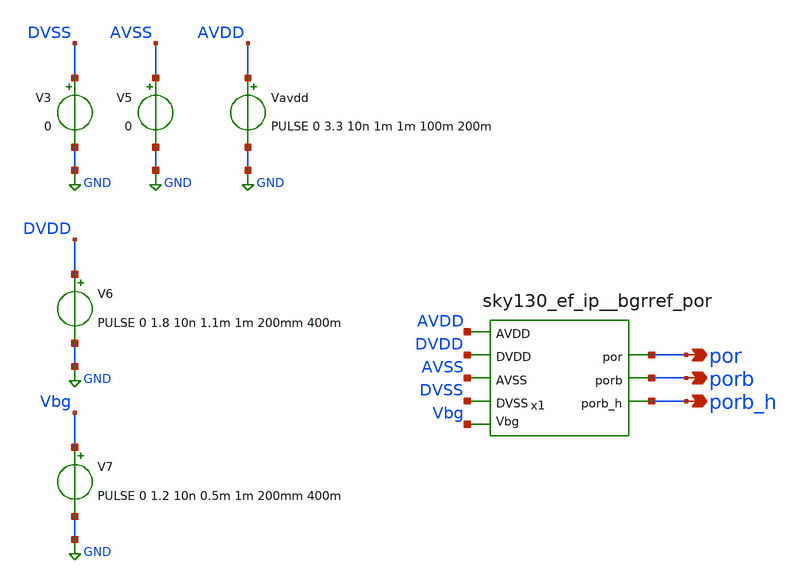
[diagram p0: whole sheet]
** sch_path: xschem/startup_sim.sch
**.subckt startup_sim por porb porb_h
*.opin por
*.opin porb
*.opin porb_h
x1 Vbg por AVSS AVDD DVDD porb DVSS porb_h VCC VSS sky130_ef_ip__bgrref_por W_N=1 L_N=0.2 W_P=1
+ L_P=0.2 m=1
V3 DVSS GND 0
Vavdd AVDD GND PULSE 0 3.3 10n 1m 1m 100m 200m
V5 AVSS GND 0
V6 DVDD GND PULSE 0 1.8 10n 1.1m 1m 200mm 400m
V7 Vbg GND PULSE 0 1.2 10n 0.5m 1m 200mm 400m
**** begin user architecture code


.options savecurrents
.control
save all
tran .5u 55m
plot AVDD por porb+6.8 porb_h+3.4
write {simpath}/{filename}.raw
*quit 0
.endc



.include {DUT_path}
.include {PDK_ROOT}/{PDK}/libs.ref/sky130_fd_sc_hvl/spice/sky130_fd_sc_hvl.spice
.include {PDK_ROOT}/{PDK}/libs.tech/combined/sky130.lib.spice {corner}
.include {PDK_ROOT}/{PDK}/libs.ref/sky130_fd_sc_hd/spice/sky130_fd_sc_hd.spice

.option TEMP={temperature}

**** end user architecture code
**.ends
.GLOBAL GND
.end
